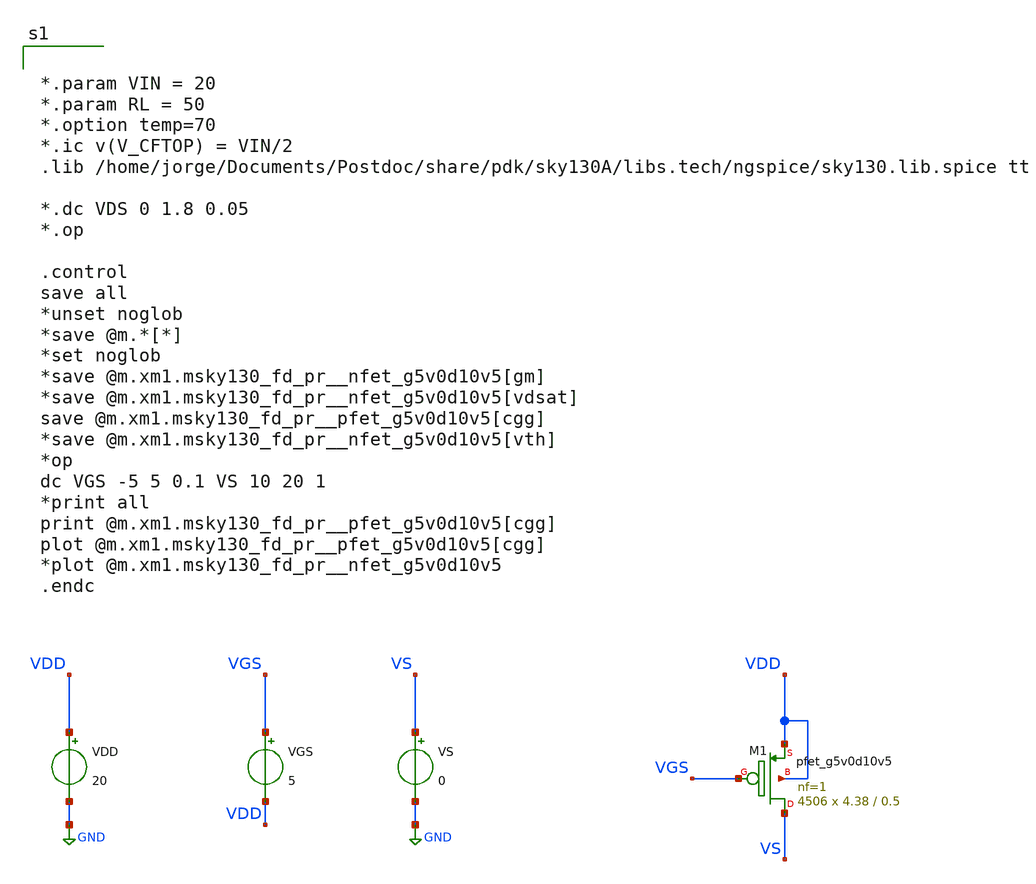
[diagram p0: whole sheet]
** sch_path: xschem/dev_switches/PMOSSW_full_OPsweep_v1p1_20220626.sch
**.subckt PMOSSW_full_OPsweep_v1p1_20220626
VGS VGS VDD 5
VS VS GND 0
VDD VDD GND 20
XM1 VS VGS VDD VDD sky130_fd_pr__pfet_g5v0d10v5 L=0.5 W=4.38 nf=1 ad='int((nf+1)/2) * W/nf * 0.29' as='int((nf+2)/2) * W/nf * 0.29'
+ pd='2*int((nf+1)/2) * (W/nf + 0.29)' ps='2*int((nf+2)/2) * (W/nf + 0.29)' nrd='0.29 / W' nrs='0.29 / W'
+ sa=0 sb=0 sd=0 mult=4506 m=4506
**** begin user architecture code


*.param VIN = 20
*.param RL = 50
*.option temp=70
*.ic v(V_CFTOP) = VIN/2
.lib /home/jorge/Documents/Postdoc/share/pdk/sky130A/libs.tech/ngspice/sky130.lib.spice tt

*.dc VDS 0 1.8 0.05
*.op

.control
save all
*unset noglob
*save @m.*[*]
*set noglob
*save @m.xm1.msky130_fd_pr__nfet_g5v0d10v5[gm]
*save @m.xm1.msky130_fd_pr__nfet_g5v0d10v5[vdsat]
save @m.xm1.msky130_fd_pr__pfet_g5v0d10v5[cgg]
*save @m.xm1.msky130_fd_pr__nfet_g5v0d10v5[vth]
*op
dc VGS -5 5 0.1 VS 10 20 1
*print all
print @m.xm1.msky130_fd_pr__pfet_g5v0d10v5[cgg]
plot @m.xm1.msky130_fd_pr__pfet_g5v0d10v5[cgg]
*plot @m.xm1.msky130_fd_pr__nfet_g5v0d10v5
.endc


**** end user architecture code
**.ends
.GLOBAL GND
.end
